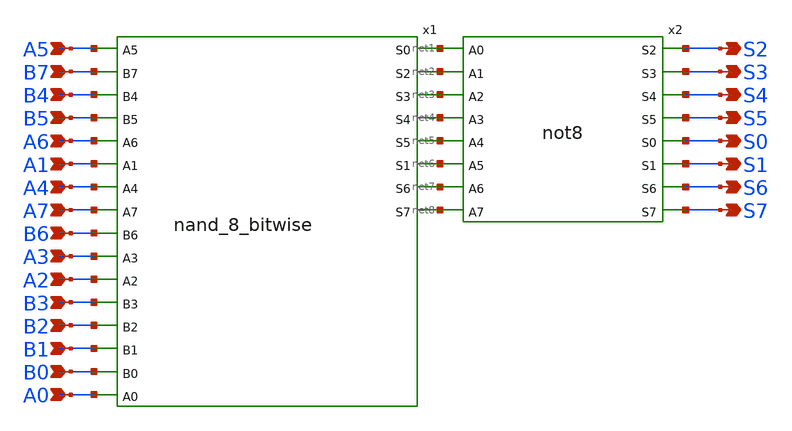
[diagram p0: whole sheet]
** sch_path: design/xschem/AND/AND.sch
**.subckt AND A0 B0 A1 B1 A2 B2 A3 B3 A4 B4 A5 B5 A6 B6 A7 B7 S0 S1 S2 S3 S4 S5 S6 S7
*.ipin A0
*.ipin B0
*.ipin A1
*.ipin B1
*.ipin A2
*.ipin B2
*.ipin A3
*.ipin B3
*.ipin A4
*.ipin B4
*.ipin A5
*.ipin B5
*.ipin A6
*.ipin B6
*.ipin A7
*.ipin B7
*.opin S0
*.opin S1
*.opin S2
*.opin S3
*.opin S4
*.opin S5
*.opin S6
*.opin S7
x1 A5 B7 B4 B5 A6 A1 A4 A7 B6 A3 A2 B3 B2 B1 B0 A0 net1 net2 net3 net4 net5 net6 net7 net8
+ nand_8_bitwise
x2 net1 net2 net3 net4 net5 net6 net7 net8 S2 S3 S4 S5 S0 S1 S6 S7 not8
**.ends
.end
